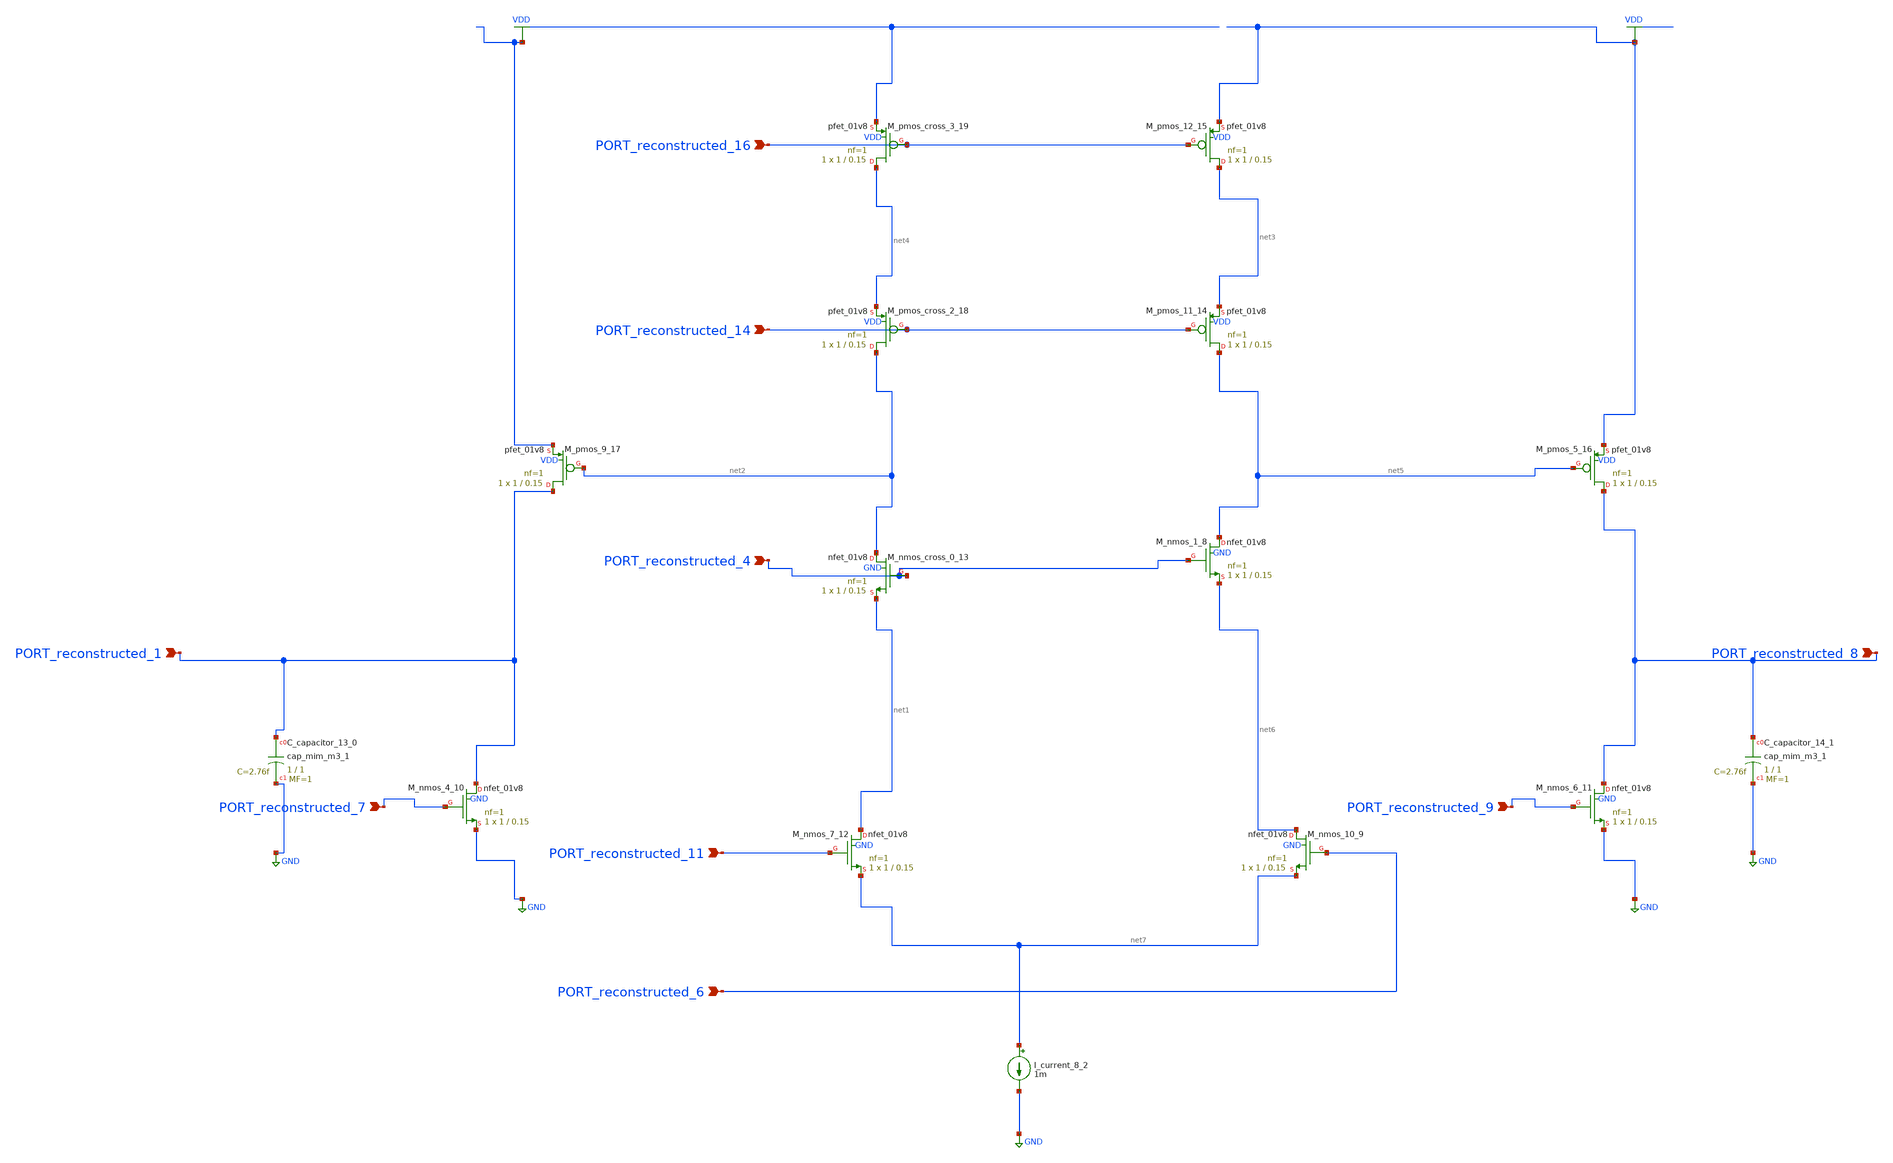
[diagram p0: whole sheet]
** sch_path: schematics/AMSNet/721.sch
**.subckt 721 PORT_reconstructed_1 PORT_reconstructed_8 PORT_reconstructed_11 PORT_reconstructed_6
*+ PORT_reconstructed_4 PORT_reconstructed_9 PORT_reconstructed_7 PORT_reconstructed_16 PORT_reconstructed_14
*.ipin PORT_reconstructed_1
*.ipin PORT_reconstructed_8
*.ipin PORT_reconstructed_11
*.ipin PORT_reconstructed_6
*.ipin PORT_reconstructed_4
*.ipin PORT_reconstructed_9
*.ipin PORT_reconstructed_7
*.ipin PORT_reconstructed_16
*.ipin PORT_reconstructed_14
XC_capacitor_13_0 PORT_reconstructed_1 GND sky130_fd_pr__cap_mim_m3_1 W=1 L=1 MF=1 m=1
XC_capacitor_14_1 PORT_reconstructed_8 GND sky130_fd_pr__cap_mim_m3_1 W=1 L=1 MF=1 m=1
I_current_8_2 net7 GND 1m
XM_nmos_1_8 net5 PORT_reconstructed_4 net6 GND sky130_fd_pr__nfet_01v8 L=0.15 W=1 nf=1 ad='int((1 + 1)/2) * 1 / 1 * 0.29'
+ as='int((1 + 2)/2) * 1 / 1 * 0.29' pd='2*int((1 + 1)/2) * (1 / 1 + 0.29)' ps='2*int((1 + 2)/2) * (1 / 1 + 0.29)'
+ nrd='0.29 / 1 ' nrs='0.29 / 1 ' sa=0 sb=0 sd=0 mult=1 m=1
XM_nmos_10_9 net6 PORT_reconstructed_6 net7 GND sky130_fd_pr__nfet_01v8 L=0.15 W=1 nf=1 ad='int((1 + 1)/2) * 1 / 1 * 0.29'
+ as='int((1 + 2)/2) * 1 / 1 * 0.29' pd='2*int((1 + 1)/2) * (1 / 1 + 0.29)' ps='2*int((1 + 2)/2) * (1 / 1 + 0.29)'
+ nrd='0.29 / 1 ' nrs='0.29 / 1 ' sa=0 sb=0 sd=0 mult=1 m=1
XM_nmos_4_10 PORT_reconstructed_1 PORT_reconstructed_7 GND GND sky130_fd_pr__nfet_01v8 L=0.15 W=1 nf=1
+ ad='int((1 + 1)/2) * 1 / 1 * 0.29' as='int((1 + 2)/2) * 1 / 1 * 0.29' pd='2*int((1 + 1)/2) * (1 / 1 + 0.29)'
+ ps='2*int((1 + 2)/2) * (1 / 1 + 0.29)' nrd='0.29 / 1 ' nrs='0.29 / 1 ' sa=0 sb=0 sd=0 mult=1 m=1
XM_nmos_6_11 PORT_reconstructed_8 PORT_reconstructed_9 GND GND sky130_fd_pr__nfet_01v8 L=0.15 W=1 nf=1
+ ad='int((1 + 1)/2) * 1 / 1 * 0.29' as='int((1 + 2)/2) * 1 / 1 * 0.29' pd='2*int((1 + 1)/2) * (1 / 1 + 0.29)'
+ ps='2*int((1 + 2)/2) * (1 / 1 + 0.29)' nrd='0.29 / 1 ' nrs='0.29 / 1 ' sa=0 sb=0 sd=0 mult=1 m=1
XM_nmos_7_12 net1 PORT_reconstructed_11 net7 GND sky130_fd_pr__nfet_01v8 L=0.15 W=1 nf=1 ad='int((1 + 1)/2) * 1 / 1 * 0.29'
+ as='int((1 + 2)/2) * 1 / 1 * 0.29' pd='2*int((1 + 1)/2) * (1 / 1 + 0.29)' ps='2*int((1 + 2)/2) * (1 / 1 + 0.29)'
+ nrd='0.29 / 1 ' nrs='0.29 / 1 ' sa=0 sb=0 sd=0 mult=1 m=1
XM_nmos_cross_0_13 net2 PORT_reconstructed_4 net1 GND sky130_fd_pr__nfet_01v8 L=0.15 W=1 nf=1 ad='int((1 + 1)/2) * 1 / 1 * 0.29'
+ as='int((1 + 2)/2) * 1 / 1 * 0.29' pd='2*int((1 + 1)/2) * (1 / 1 + 0.29)' ps='2*int((1 + 2)/2) * (1 / 1 + 0.29)'
+ nrd='0.29 / 1 ' nrs='0.29 / 1 ' sa=0 sb=0 sd=0 mult=1 m=1
XM_pmos_11_14 net5 PORT_reconstructed_14 net3 VDD sky130_fd_pr__pfet_01v8 L=0.15 W=1 nf=1 ad='int((1 + 1)/2) * 1 / 1 * 0.29'
+ as='int((1 + 2)/2) * 1 / 1 * 0.29' pd='2*int((1 + 1)/2) * (1 / 1 + 0.29)' ps='2*int((1 + 2)/2) * (1 / 1 + 0.29)'
+ nrd='0.29 / 1 ' nrs='0.29 / 1 ' sa=0 sb=0 sd=0 mult=1 m=1
XM_pmos_12_15 net3 PORT_reconstructed_16 VDD VDD sky130_fd_pr__pfet_01v8 L=0.15 W=1 nf=1 ad='int((1 + 1)/2) * 1 / 1 * 0.29'
+ as='int((1 + 2)/2) * 1 / 1 * 0.29' pd='2*int((1 + 1)/2) * (1 / 1 + 0.29)' ps='2*int((1 + 2)/2) * (1 / 1 + 0.29)'
+ nrd='0.29 / 1 ' nrs='0.29 / 1 ' sa=0 sb=0 sd=0 mult=1 m=1
XM_pmos_5_16 PORT_reconstructed_8 net5 VDD VDD sky130_fd_pr__pfet_01v8 L=0.15 W=1 nf=1 ad='int((1 + 1)/2) * 1 / 1 * 0.29'
+ as='int((1 + 2)/2) * 1 / 1 * 0.29' pd='2*int((1 + 1)/2) * (1 / 1 + 0.29)' ps='2*int((1 + 2)/2) * (1 / 1 + 0.29)'
+ nrd='0.29 / 1 ' nrs='0.29 / 1 ' sa=0 sb=0 sd=0 mult=1 m=1
XM_pmos_9_17 PORT_reconstructed_1 net2 VDD VDD sky130_fd_pr__pfet_01v8 L=0.15 W=1 nf=1 ad='int((1 + 1)/2) * 1 / 1 * 0.29'
+ as='int((1 + 2)/2) * 1 / 1 * 0.29' pd='2*int((1 + 1)/2) * (1 / 1 + 0.29)' ps='2*int((1 + 2)/2) * (1 / 1 + 0.29)'
+ nrd='0.29 / 1 ' nrs='0.29 / 1 ' sa=0 sb=0 sd=0 mult=1 m=1
XM_pmos_cross_2_18 net2 PORT_reconstructed_14 net4 VDD sky130_fd_pr__pfet_01v8 L=0.15 W=1 nf=1 ad='int((1 + 1)/2) * 1 / 1 * 0.29'
+ as='int((1 + 2)/2) * 1 / 1 * 0.29' pd='2*int((1 + 1)/2) * (1 / 1 + 0.29)' ps='2*int((1 + 2)/2) * (1 / 1 + 0.29)'
+ nrd='0.29 / 1 ' nrs='0.29 / 1 ' sa=0 sb=0 sd=0 mult=1 m=1
XM_pmos_cross_3_19 net4 PORT_reconstructed_16 VDD VDD sky130_fd_pr__pfet_01v8 L=0.15 W=1 nf=1 ad='int((1 + 1)/2) * 1 / 1 * 0.29'
+ as='int((1 + 2)/2) * 1 / 1 * 0.29' pd='2*int((1 + 1)/2) * (1 / 1 + 0.29)' ps='2*int((1 + 2)/2) * (1 / 1 + 0.29)'
+ nrd='0.29 / 1 ' nrs='0.29 / 1 ' sa=0 sb=0 sd=0 mult=1 m=1
**.ends
.GLOBAL GND
.GLOBAL VDD
.end
